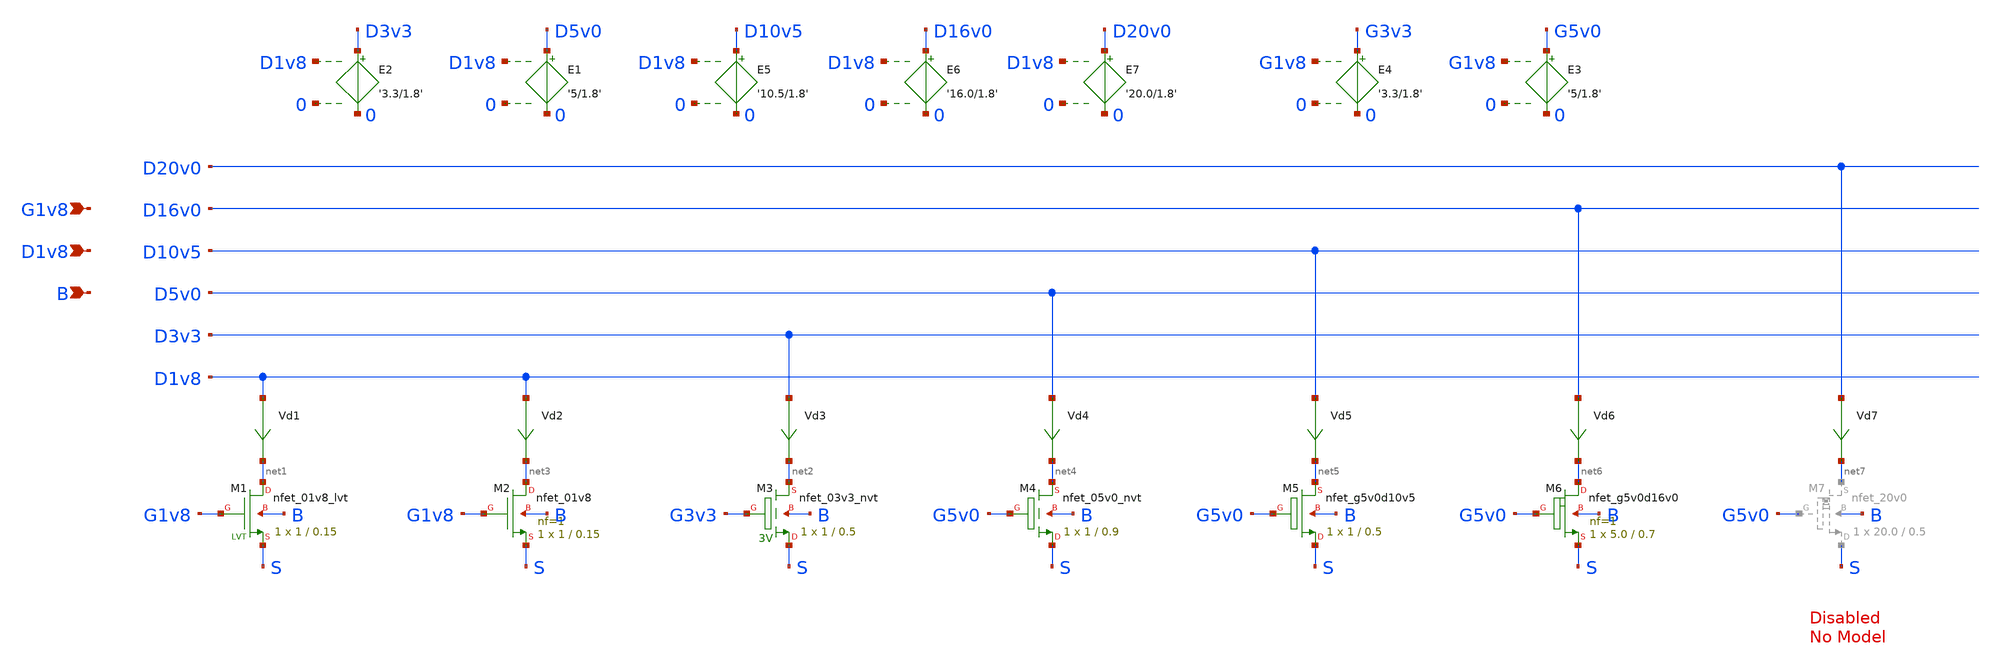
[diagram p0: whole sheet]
** sch_path: sky130_tests/test_nmos.sch
* Copyright 2020 Stefan Frederik Schippers
* Licensed under the Apache License, Version 2.0 (the "License");
* you may not use this file except in compliance with the License.
* You may obtain a copy of the License at
* https://www.apache.org/licenses/LICENSE-2.0
* Unless required by applicable law or agreed to in writing, software
* distributed under the License is distributed on an "AS IS" BASIS,
* WITHOUT WARRANTIES OR CONDITIONS OF ANY KIND, either express or implied.
* See the License for the specific language governing permissions and
* limitations under the License.
**.subckt test_nmos G1v8 D1v8 B
*.ipin G1v8
*.ipin D1v8
*.ipin B
Vd1 D1v8 net1 0
.save i(vd1)
Vd3 D3v3 net2 0
.save i(vd3)
XM2 net3 G1v8 S B sky130_fd_pr__nfet_01v8 L=0.15 W=1 nf=1 ad='int((1 + 1)/2) * 1 / 1 * 0.29' as='int((1 + 2)/2) * 1 / 1 * 0.29'
+ pd='2*int((1 + 1)/2) * (1 / 1 + 0.29)' ps='2*int((1 + 2)/2) * (1 / 1 + 0.29)' nrd='0.29 / 1 ' nrs='0.29 / 1 '
+ sa=0 sb=0 sd=0 mult=1 m=1
Vd2 D1v8 net3 0
.save i(vd2)
XM3 net2 G3v3 S B sky130_fd_pr__nfet_03v3_nvt W=1 L=0.5 ad='W * 0.29' pd='W + 2 * 0.29' as='W * 0.29'
+ ps='W + 2 * 0.29' nrd=0 nrs=0 sa=0 sb=0 sd=0 nf=1 mult=1
Vd4 D5v0 net4 0
.save i(vd4)
XM4 net4 G5v0 S B sky130_fd_pr__nfet_05v0_nvt W=1 L=0.9 ad='W * 0.29' pd='W + 2 * 0.29' as='W * 0.29'
+ ps='W + 2 * 0.29' nrd=0 nrs=0 sa=0 sb=0 sd=0 nf=1 mult=1 m=1
E1 D5v0 0 D1v8 0 '5/1.8'
E2 D3v3 0 D1v8 0 '3.3/1.8'
E3 G5v0 0 G1v8 0 '5/1.8'
E4 G3v3 0 G1v8 0 '3.3/1.8'
Vd5 D10v5 net5 0
.save i(vd5)
E5 D10v5 0 D1v8 0 '10.5/1.8'
XM5 net5 G5v0 S B sky130_fd_pr__nfet_g5v0d10v5 W=1 L=0.5 ad='W * 0.29' pd='W + 2 * 0.29' as='W * 0.29'
+ ps='W + 2 * 0.29' nrd=0 nrs=0 sa=0 sb=0 sd=0 nf=1 mult=1
E6 D16v0 0 D1v8 0 '16.0/1.8'
Vd6 D16v0 net6 0
.save i(vd6)
XM6 net6 G5v0 S B sky130_fd_pr__nfet_g5v0d16v0 L=0.7 W=5.0 nf=1 ad='W * 0.29' as='W * 0.29' pd='W + 2 * 0.29'
+ ps='W + 2 * 0.29' nrd=0 nrs=0 sa=0 sb=0 sd=0 mult=1 m=1
Vd7 D20v0 net7 0
.save i(vd7)
E7 D20v0 0 D1v8 0 '20.0/1.8'
XM1 net1 G1v8 S B sky130_fd_pr__nfet_01v8_lvt W=1 L=0.15 ad='W * 0.29' pd='2 * (W + 0.29)' as='W * 0.29'
+ ps='2 * (W + 0.29)' nrd='0.29 / W' nrs='0.29 / W' sa=0 sb=0 sd=0 nf=1 mult=1 m=1
**** begin user architecture code


vg G1v8 0 0
vs s 0 0
vd D1v8 0 0
vb b 0 0
.control
dc vd 0 1.8 0.01 vg 0 1.8 0.2
* plot all.vd1#branch vs D1v8
* plot all.vd2#branch vs D1v8
* plot all.vd3#branch vs D3v3
plot all.vd4#branch vs D5v0
plot all.vd5#branch vs D10v5
plot all.vd6#branch vs D16v0
plot all.vd7#branch vs D20v0
.endc


eval(
**** end user architecture code
**.ends
.end
